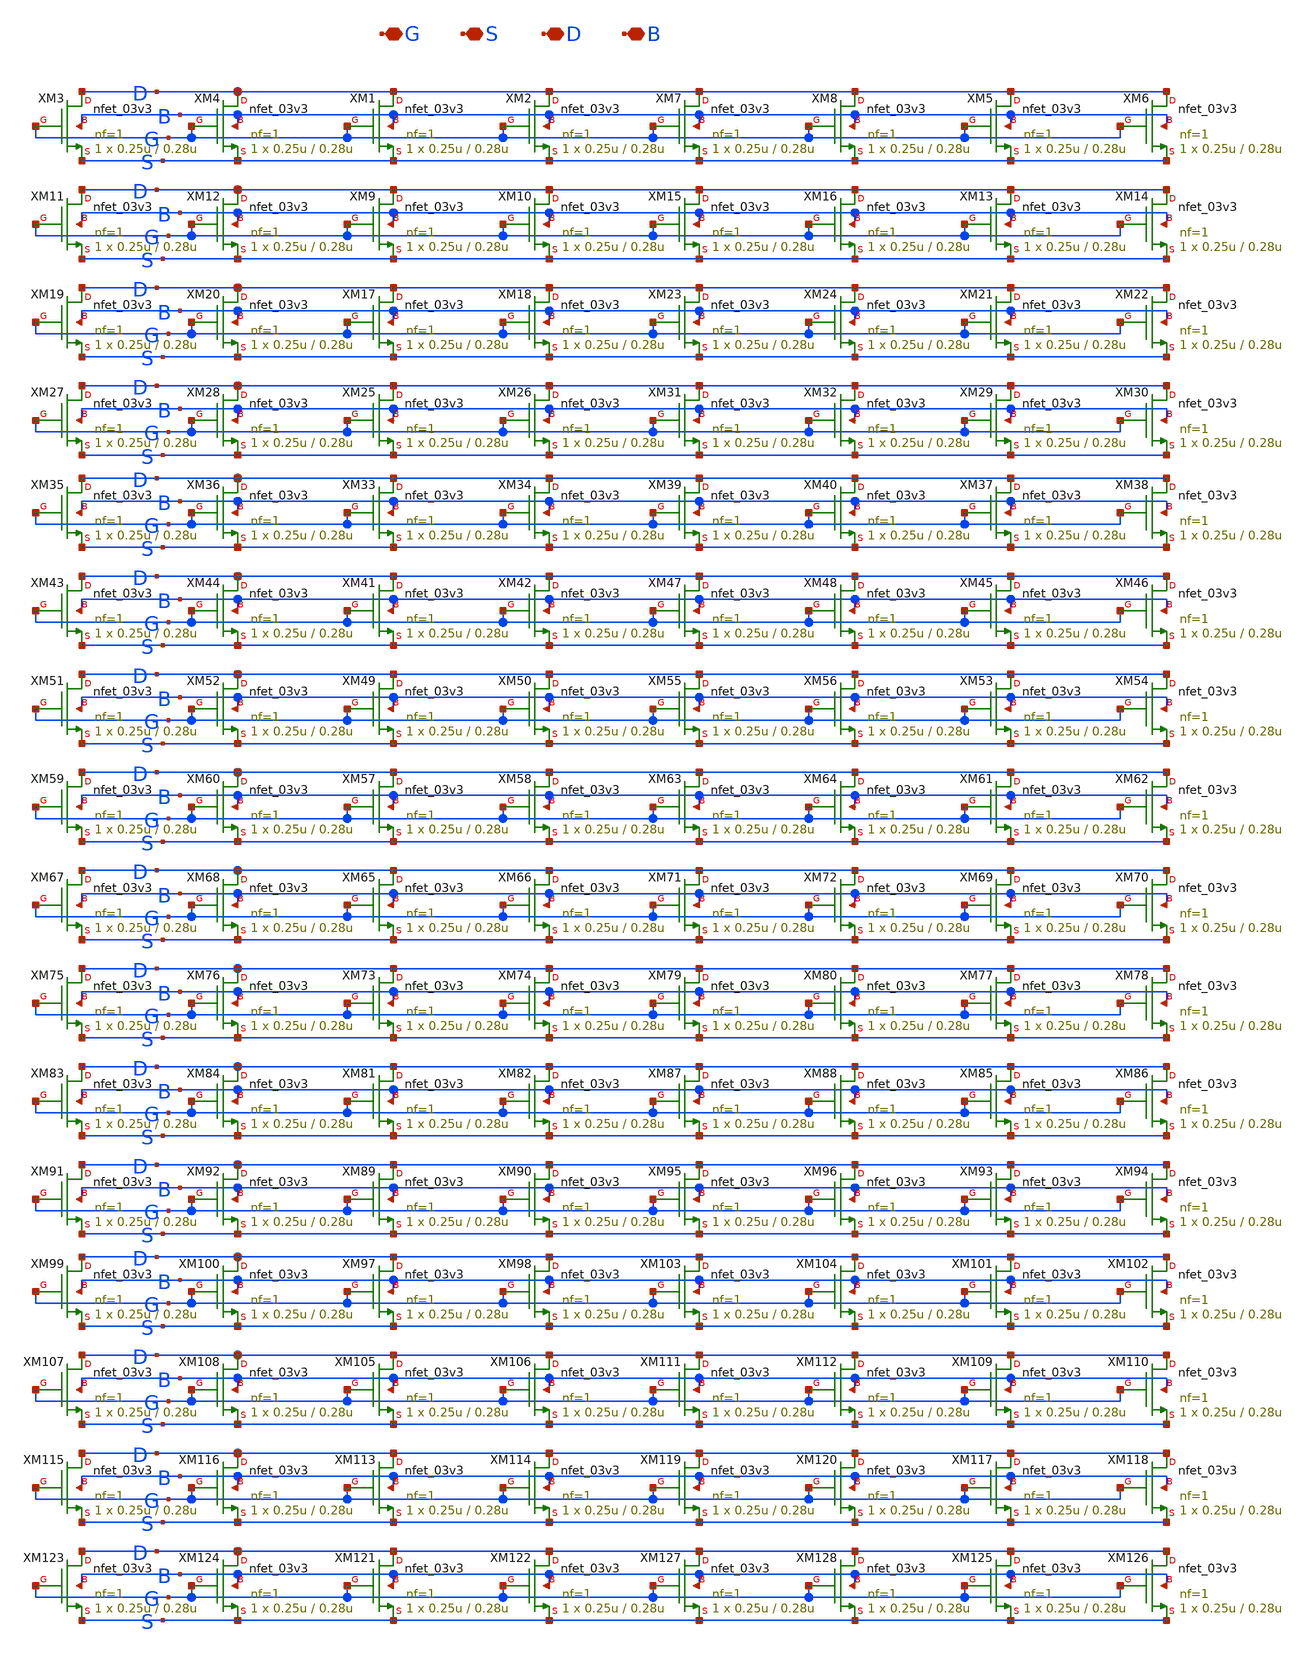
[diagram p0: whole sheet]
** sch_path: DAC_PAKISTAN_01/Pakistan1_Xschem/nfet_03V3_m128.sch
**.subckt nfet_03V3_m128 G S D B
*.iopin G
*.iopin S
*.iopin D
*.iopin B
XM1 D G S B nfet_03v3 L=0.28u W=0.25u nf=1 ad='int((nf+1)/2) * W/nf * 0.18u' as='int((nf+2)/2) * W/nf * 0.18u'
+ pd='2*int((nf+1)/2) * (W/nf + 0.18u)' ps='2*int((nf+2)/2) * (W/nf + 0.18u)' nrd='0.18u / W' nrs='0.18u / W'
+ sa=0 sb=0 sd=0 m=1
XM2 D G S B nfet_03v3 L=0.28u W=0.25u nf=1 ad='int((nf+1)/2) * W/nf * 0.18u' as='int((nf+2)/2) * W/nf * 0.18u'
+ pd='2*int((nf+1)/2) * (W/nf + 0.18u)' ps='2*int((nf+2)/2) * (W/nf + 0.18u)' nrd='0.18u / W' nrs='0.18u / W'
+ sa=0 sb=0 sd=0 m=1
XM3 D G S B nfet_03v3 L=0.28u W=0.25u nf=1 ad='int((nf+1)/2) * W/nf * 0.18u' as='int((nf+2)/2) * W/nf * 0.18u'
+ pd='2*int((nf+1)/2) * (W/nf + 0.18u)' ps='2*int((nf+2)/2) * (W/nf + 0.18u)' nrd='0.18u / W' nrs='0.18u / W'
+ sa=0 sb=0 sd=0 m=1
XM4 D G S B nfet_03v3 L=0.28u W=0.25u nf=1 ad='int((nf+1)/2) * W/nf * 0.18u' as='int((nf+2)/2) * W/nf * 0.18u'
+ pd='2*int((nf+1)/2) * (W/nf + 0.18u)' ps='2*int((nf+2)/2) * (W/nf + 0.18u)' nrd='0.18u / W' nrs='0.18u / W'
+ sa=0 sb=0 sd=0 m=1
XM5 D G S B nfet_03v3 L=0.28u W=0.25u nf=1 ad='int((nf+1)/2) * W/nf * 0.18u' as='int((nf+2)/2) * W/nf * 0.18u'
+ pd='2*int((nf+1)/2) * (W/nf + 0.18u)' ps='2*int((nf+2)/2) * (W/nf + 0.18u)' nrd='0.18u / W' nrs='0.18u / W'
+ sa=0 sb=0 sd=0 m=1
XM6 D G S B nfet_03v3 L=0.28u W=0.25u nf=1 ad='int((nf+1)/2) * W/nf * 0.18u' as='int((nf+2)/2) * W/nf * 0.18u'
+ pd='2*int((nf+1)/2) * (W/nf + 0.18u)' ps='2*int((nf+2)/2) * (W/nf + 0.18u)' nrd='0.18u / W' nrs='0.18u / W'
+ sa=0 sb=0 sd=0 m=1
XM7 D G S B nfet_03v3 L=0.28u W=0.25u nf=1 ad='int((nf+1)/2) * W/nf * 0.18u' as='int((nf+2)/2) * W/nf * 0.18u'
+ pd='2*int((nf+1)/2) * (W/nf + 0.18u)' ps='2*int((nf+2)/2) * (W/nf + 0.18u)' nrd='0.18u / W' nrs='0.18u / W'
+ sa=0 sb=0 sd=0 m=1
XM8 D G S B nfet_03v3 L=0.28u W=0.25u nf=1 ad='int((nf+1)/2) * W/nf * 0.18u' as='int((nf+2)/2) * W/nf * 0.18u'
+ pd='2*int((nf+1)/2) * (W/nf + 0.18u)' ps='2*int((nf+2)/2) * (W/nf + 0.18u)' nrd='0.18u / W' nrs='0.18u / W'
+ sa=0 sb=0 sd=0 m=1
XM9 D G S B nfet_03v3 L=0.28u W=0.25u nf=1 ad='int((nf+1)/2) * W/nf * 0.18u' as='int((nf+2)/2) * W/nf * 0.18u'
+ pd='2*int((nf+1)/2) * (W/nf + 0.18u)' ps='2*int((nf+2)/2) * (W/nf + 0.18u)' nrd='0.18u / W' nrs='0.18u / W'
+ sa=0 sb=0 sd=0 m=1
XM10 D G S B nfet_03v3 L=0.28u W=0.25u nf=1 ad='int((nf+1)/2) * W/nf * 0.18u' as='int((nf+2)/2) * W/nf * 0.18u'
+ pd='2*int((nf+1)/2) * (W/nf + 0.18u)' ps='2*int((nf+2)/2) * (W/nf + 0.18u)' nrd='0.18u / W' nrs='0.18u / W'
+ sa=0 sb=0 sd=0 m=1
XM11 D G S B nfet_03v3 L=0.28u W=0.25u nf=1 ad='int((nf+1)/2) * W/nf * 0.18u' as='int((nf+2)/2) * W/nf * 0.18u'
+ pd='2*int((nf+1)/2) * (W/nf + 0.18u)' ps='2*int((nf+2)/2) * (W/nf + 0.18u)' nrd='0.18u / W' nrs='0.18u / W'
+ sa=0 sb=0 sd=0 m=1
XM12 D G S B nfet_03v3 L=0.28u W=0.25u nf=1 ad='int((nf+1)/2) * W/nf * 0.18u' as='int((nf+2)/2) * W/nf * 0.18u'
+ pd='2*int((nf+1)/2) * (W/nf + 0.18u)' ps='2*int((nf+2)/2) * (W/nf + 0.18u)' nrd='0.18u / W' nrs='0.18u / W'
+ sa=0 sb=0 sd=0 m=1
XM13 D G S B nfet_03v3 L=0.28u W=0.25u nf=1 ad='int((nf+1)/2) * W/nf * 0.18u' as='int((nf+2)/2) * W/nf * 0.18u'
+ pd='2*int((nf+1)/2) * (W/nf + 0.18u)' ps='2*int((nf+2)/2) * (W/nf + 0.18u)' nrd='0.18u / W' nrs='0.18u / W'
+ sa=0 sb=0 sd=0 m=1
XM14 D G S B nfet_03v3 L=0.28u W=0.25u nf=1 ad='int((nf+1)/2) * W/nf * 0.18u' as='int((nf+2)/2) * W/nf * 0.18u'
+ pd='2*int((nf+1)/2) * (W/nf + 0.18u)' ps='2*int((nf+2)/2) * (W/nf + 0.18u)' nrd='0.18u / W' nrs='0.18u / W'
+ sa=0 sb=0 sd=0 m=1
XM15 D G S B nfet_03v3 L=0.28u W=0.25u nf=1 ad='int((nf+1)/2) * W/nf * 0.18u' as='int((nf+2)/2) * W/nf * 0.18u'
+ pd='2*int((nf+1)/2) * (W/nf + 0.18u)' ps='2*int((nf+2)/2) * (W/nf + 0.18u)' nrd='0.18u / W' nrs='0.18u / W'
+ sa=0 sb=0 sd=0 m=1
XM16 D G S B nfet_03v3 L=0.28u W=0.25u nf=1 ad='int((nf+1)/2) * W/nf * 0.18u' as='int((nf+2)/2) * W/nf * 0.18u'
+ pd='2*int((nf+1)/2) * (W/nf + 0.18u)' ps='2*int((nf+2)/2) * (W/nf + 0.18u)' nrd='0.18u / W' nrs='0.18u / W'
+ sa=0 sb=0 sd=0 m=1
XM17 D G S B nfet_03v3 L=0.28u W=0.25u nf=1 ad='int((nf+1)/2) * W/nf * 0.18u' as='int((nf+2)/2) * W/nf * 0.18u'
+ pd='2*int((nf+1)/2) * (W/nf + 0.18u)' ps='2*int((nf+2)/2) * (W/nf + 0.18u)' nrd='0.18u / W' nrs='0.18u / W'
+ sa=0 sb=0 sd=0 m=1
XM18 D G S B nfet_03v3 L=0.28u W=0.25u nf=1 ad='int((nf+1)/2) * W/nf * 0.18u' as='int((nf+2)/2) * W/nf * 0.18u'
+ pd='2*int((nf+1)/2) * (W/nf + 0.18u)' ps='2*int((nf+2)/2) * (W/nf + 0.18u)' nrd='0.18u / W' nrs='0.18u / W'
+ sa=0 sb=0 sd=0 m=1
XM19 D G S B nfet_03v3 L=0.28u W=0.25u nf=1 ad='int((nf+1)/2) * W/nf * 0.18u' as='int((nf+2)/2) * W/nf * 0.18u'
+ pd='2*int((nf+1)/2) * (W/nf + 0.18u)' ps='2*int((nf+2)/2) * (W/nf + 0.18u)' nrd='0.18u / W' nrs='0.18u / W'
+ sa=0 sb=0 sd=0 m=1
XM20 D G S B nfet_03v3 L=0.28u W=0.25u nf=1 ad='int((nf+1)/2) * W/nf * 0.18u' as='int((nf+2)/2) * W/nf * 0.18u'
+ pd='2*int((nf+1)/2) * (W/nf + 0.18u)' ps='2*int((nf+2)/2) * (W/nf + 0.18u)' nrd='0.18u / W' nrs='0.18u / W'
+ sa=0 sb=0 sd=0 m=1
XM21 D G S B nfet_03v3 L=0.28u W=0.25u nf=1 ad='int((nf+1)/2) * W/nf * 0.18u' as='int((nf+2)/2) * W/nf * 0.18u'
+ pd='2*int((nf+1)/2) * (W/nf + 0.18u)' ps='2*int((nf+2)/2) * (W/nf + 0.18u)' nrd='0.18u / W' nrs='0.18u / W'
+ sa=0 sb=0 sd=0 m=1
XM22 D G S B nfet_03v3 L=0.28u W=0.25u nf=1 ad='int((nf+1)/2) * W/nf * 0.18u' as='int((nf+2)/2) * W/nf * 0.18u'
+ pd='2*int((nf+1)/2) * (W/nf + 0.18u)' ps='2*int((nf+2)/2) * (W/nf + 0.18u)' nrd='0.18u / W' nrs='0.18u / W'
+ sa=0 sb=0 sd=0 m=1
XM23 D G S B nfet_03v3 L=0.28u W=0.25u nf=1 ad='int((nf+1)/2) * W/nf * 0.18u' as='int((nf+2)/2) * W/nf * 0.18u'
+ pd='2*int((nf+1)/2) * (W/nf + 0.18u)' ps='2*int((nf+2)/2) * (W/nf + 0.18u)' nrd='0.18u / W' nrs='0.18u / W'
+ sa=0 sb=0 sd=0 m=1
XM24 D G S B nfet_03v3 L=0.28u W=0.25u nf=1 ad='int((nf+1)/2) * W/nf * 0.18u' as='int((nf+2)/2) * W/nf * 0.18u'
+ pd='2*int((nf+1)/2) * (W/nf + 0.18u)' ps='2*int((nf+2)/2) * (W/nf + 0.18u)' nrd='0.18u / W' nrs='0.18u / W'
+ sa=0 sb=0 sd=0 m=1
XM25 D G S B nfet_03v3 L=0.28u W=0.25u nf=1 ad='int((nf+1)/2) * W/nf * 0.18u' as='int((nf+2)/2) * W/nf * 0.18u'
+ pd='2*int((nf+1)/2) * (W/nf + 0.18u)' ps='2*int((nf+2)/2) * (W/nf + 0.18u)' nrd='0.18u / W' nrs='0.18u / W'
+ sa=0 sb=0 sd=0 m=1
XM26 D G S B nfet_03v3 L=0.28u W=0.25u nf=1 ad='int((nf+1)/2) * W/nf * 0.18u' as='int((nf+2)/2) * W/nf * 0.18u'
+ pd='2*int((nf+1)/2) * (W/nf + 0.18u)' ps='2*int((nf+2)/2) * (W/nf + 0.18u)' nrd='0.18u / W' nrs='0.18u / W'
+ sa=0 sb=0 sd=0 m=1
XM27 D G S B nfet_03v3 L=0.28u W=0.25u nf=1 ad='int((nf+1)/2) * W/nf * 0.18u' as='int((nf+2)/2) * W/nf * 0.18u'
+ pd='2*int((nf+1)/2) * (W/nf + 0.18u)' ps='2*int((nf+2)/2) * (W/nf + 0.18u)' nrd='0.18u / W' nrs='0.18u / W'
+ sa=0 sb=0 sd=0 m=1
XM28 D G S B nfet_03v3 L=0.28u W=0.25u nf=1 ad='int((nf+1)/2) * W/nf * 0.18u' as='int((nf+2)/2) * W/nf * 0.18u'
+ pd='2*int((nf+1)/2) * (W/nf + 0.18u)' ps='2*int((nf+2)/2) * (W/nf + 0.18u)' nrd='0.18u / W' nrs='0.18u / W'
+ sa=0 sb=0 sd=0 m=1
XM29 D G S B nfet_03v3 L=0.28u W=0.25u nf=1 ad='int((nf+1)/2) * W/nf * 0.18u' as='int((nf+2)/2) * W/nf * 0.18u'
+ pd='2*int((nf+1)/2) * (W/nf + 0.18u)' ps='2*int((nf+2)/2) * (W/nf + 0.18u)' nrd='0.18u / W' nrs='0.18u / W'
+ sa=0 sb=0 sd=0 m=1
XM30 D G S B nfet_03v3 L=0.28u W=0.25u nf=1 ad='int((nf+1)/2) * W/nf * 0.18u' as='int((nf+2)/2) * W/nf * 0.18u'
+ pd='2*int((nf+1)/2) * (W/nf + 0.18u)' ps='2*int((nf+2)/2) * (W/nf + 0.18u)' nrd='0.18u / W' nrs='0.18u / W'
+ sa=0 sb=0 sd=0 m=1
XM31 D G S B nfet_03v3 L=0.28u W=0.25u nf=1 ad='int((nf+1)/2) * W/nf * 0.18u' as='int((nf+2)/2) * W/nf * 0.18u'
+ pd='2*int((nf+1)/2) * (W/nf + 0.18u)' ps='2*int((nf+2)/2) * (W/nf + 0.18u)' nrd='0.18u / W' nrs='0.18u / W'
+ sa=0 sb=0 sd=0 m=1
XM32 D G S B nfet_03v3 L=0.28u W=0.25u nf=1 ad='int((nf+1)/2) * W/nf * 0.18u' as='int((nf+2)/2) * W/nf * 0.18u'
+ pd='2*int((nf+1)/2) * (W/nf + 0.18u)' ps='2*int((nf+2)/2) * (W/nf + 0.18u)' nrd='0.18u / W' nrs='0.18u / W'
+ sa=0 sb=0 sd=0 m=1
XM33 D G S B nfet_03v3 L=0.28u W=0.25u nf=1 ad='int((nf+1)/2) * W/nf * 0.18u' as='int((nf+2)/2) * W/nf * 0.18u'
+ pd='2*int((nf+1)/2) * (W/nf + 0.18u)' ps='2*int((nf+2)/2) * (W/nf + 0.18u)' nrd='0.18u / W' nrs='0.18u / W'
+ sa=0 sb=0 sd=0 m=1
XM34 D G S B nfet_03v3 L=0.28u W=0.25u nf=1 ad='int((nf+1)/2) * W/nf * 0.18u' as='int((nf+2)/2) * W/nf * 0.18u'
+ pd='2*int((nf+1)/2) * (W/nf + 0.18u)' ps='2*int((nf+2)/2) * (W/nf + 0.18u)' nrd='0.18u / W' nrs='0.18u / W'
+ sa=0 sb=0 sd=0 m=1
XM35 D G S B nfet_03v3 L=0.28u W=0.25u nf=1 ad='int((nf+1)/2) * W/nf * 0.18u' as='int((nf+2)/2) * W/nf * 0.18u'
+ pd='2*int((nf+1)/2) * (W/nf + 0.18u)' ps='2*int((nf+2)/2) * (W/nf + 0.18u)' nrd='0.18u / W' nrs='0.18u / W'
+ sa=0 sb=0 sd=0 m=1
XM36 D G S B nfet_03v3 L=0.28u W=0.25u nf=1 ad='int((nf+1)/2) * W/nf * 0.18u' as='int((nf+2)/2) * W/nf * 0.18u'
+ pd='2*int((nf+1)/2) * (W/nf + 0.18u)' ps='2*int((nf+2)/2) * (W/nf + 0.18u)' nrd='0.18u / W' nrs='0.18u / W'
+ sa=0 sb=0 sd=0 m=1
XM37 D G S B nfet_03v3 L=0.28u W=0.25u nf=1 ad='int((nf+1)/2) * W/nf * 0.18u' as='int((nf+2)/2) * W/nf * 0.18u'
+ pd='2*int((nf+1)/2) * (W/nf + 0.18u)' ps='2*int((nf+2)/2) * (W/nf + 0.18u)' nrd='0.18u / W' nrs='0.18u / W'
+ sa=0 sb=0 sd=0 m=1
XM38 D G S B nfet_03v3 L=0.28u W=0.25u nf=1 ad='int((nf+1)/2) * W/nf * 0.18u' as='int((nf+2)/2) * W/nf * 0.18u'
+ pd='2*int((nf+1)/2) * (W/nf + 0.18u)' ps='2*int((nf+2)/2) * (W/nf + 0.18u)' nrd='0.18u / W' nrs='0.18u / W'
+ sa=0 sb=0 sd=0 m=1
XM39 D G S B nfet_03v3 L=0.28u W=0.25u nf=1 ad='int((nf+1)/2) * W/nf * 0.18u' as='int((nf+2)/2) * W/nf * 0.18u'
+ pd='2*int((nf+1)/2) * (W/nf + 0.18u)' ps='2*int((nf+2)/2) * (W/nf + 0.18u)' nrd='0.18u / W' nrs='0.18u / W'
+ sa=0 sb=0 sd=0 m=1
XM40 D G S B nfet_03v3 L=0.28u W=0.25u nf=1 ad='int((nf+1)/2) * W/nf * 0.18u' as='int((nf+2)/2) * W/nf * 0.18u'
+ pd='2*int((nf+1)/2) * (W/nf + 0.18u)' ps='2*int((nf+2)/2) * (W/nf + 0.18u)' nrd='0.18u / W' nrs='0.18u / W'
+ sa=0 sb=0 sd=0 m=1
XM41 D G S B nfet_03v3 L=0.28u W=0.25u nf=1 ad='int((nf+1)/2) * W/nf * 0.18u' as='int((nf+2)/2) * W/nf * 0.18u'
+ pd='2*int((nf+1)/2) * (W/nf + 0.18u)' ps='2*int((nf+2)/2) * (W/nf + 0.18u)' nrd='0.18u / W' nrs='0.18u / W'
+ sa=0 sb=0 sd=0 m=1
XM42 D G S B nfet_03v3 L=0.28u W=0.25u nf=1 ad='int((nf+1)/2) * W/nf * 0.18u' as='int((nf+2)/2) * W/nf * 0.18u'
+ pd='2*int((nf+1)/2) * (W/nf + 0.18u)' ps='2*int((nf+2)/2) * (W/nf + 0.18u)' nrd='0.18u / W' nrs='0.18u / W'
+ sa=0 sb=0 sd=0 m=1
XM43 D G S B nfet_03v3 L=0.28u W=0.25u nf=1 ad='int((nf+1)/2) * W/nf * 0.18u' as='int((nf+2)/2) * W/nf * 0.18u'
+ pd='2*int((nf+1)/2) * (W/nf + 0.18u)' ps='2*int((nf+2)/2) * (W/nf + 0.18u)' nrd='0.18u / W' nrs='0.18u / W'
+ sa=0 sb=0 sd=0 m=1
XM44 D G S B nfet_03v3 L=0.28u W=0.25u nf=1 ad='int((nf+1)/2) * W/nf * 0.18u' as='int((nf+2)/2) * W/nf * 0.18u'
+ pd='2*int((nf+1)/2) * (W/nf + 0.18u)' ps='2*int((nf+2)/2) * (W/nf + 0.18u)' nrd='0.18u / W' nrs='0.18u / W'
+ sa=0 sb=0 sd=0 m=1
XM45 D G S B nfet_03v3 L=0.28u W=0.25u nf=1 ad='int((nf+1)/2) * W/nf * 0.18u' as='int((nf+2)/2) * W/nf * 0.18u'
+ pd='2*int((nf+1)/2) * (W/nf + 0.18u)' ps='2*int((nf+2)/2) * (W/nf + 0.18u)' nrd='0.18u / W' nrs='0.18u / W'
+ sa=0 sb=0 sd=0 m=1
XM46 D G S B nfet_03v3 L=0.28u W=0.25u nf=1 ad='int((nf+1)/2) * W/nf * 0.18u' as='int((nf+2)/2) * W/nf * 0.18u'
+ pd='2*int((nf+1)/2) * (W/nf + 0.18u)' ps='2*int((nf+2)/2) * (W/nf + 0.18u)' nrd='0.18u / W' nrs='0.18u / W'
+ sa=0 sb=0 sd=0 m=1
XM47 D G S B nfet_03v3 L=0.28u W=0.25u nf=1 ad='int((nf+1)/2) * W/nf * 0.18u' as='int((nf+2)/2) * W/nf * 0.18u'
+ pd='2*int((nf+1)/2) * (W/nf + 0.18u)' ps='2*int((nf+2)/2) * (W/nf + 0.18u)' nrd='0.18u / W' nrs='0.18u / W'
+ sa=0 sb=0 sd=0 m=1
XM48 D G S B nfet_03v3 L=0.28u W=0.25u nf=1 ad='int((nf+1)/2) * W/nf * 0.18u' as='int((nf+2)/2) * W/nf * 0.18u'
+ pd='2*int((nf+1)/2) * (W/nf + 0.18u)' ps='2*int((nf+2)/2) * (W/nf + 0.18u)' nrd='0.18u / W' nrs='0.18u / W'
+ sa=0 sb=0 sd=0 m=1
XM49 D G S B nfet_03v3 L=0.28u W=0.25u nf=1 ad='int((nf+1)/2) * W/nf * 0.18u' as='int((nf+2)/2) * W/nf * 0.18u'
+ pd='2*int((nf+1)/2) * (W/nf + 0.18u)' ps='2*int((nf+2)/2) * (W/nf + 0.18u)' nrd='0.18u / W' nrs='0.18u / W'
+ sa=0 sb=0 sd=0 m=1
XM50 D G S B nfet_03v3 L=0.28u W=0.25u nf=1 ad='int((nf+1)/2) * W/nf * 0.18u' as='int((nf+2)/2) * W/nf * 0.18u'
+ pd='2*int((nf+1)/2) * (W/nf + 0.18u)' ps='2*int((nf+2)/2) * (W/nf + 0.18u)' nrd='0.18u / W' nrs='0.18u / W'
+ sa=0 sb=0 sd=0 m=1
XM51 D G S B nfet_03v3 L=0.28u W=0.25u nf=1 ad='int((nf+1)/2) * W/nf * 0.18u' as='int((nf+2)/2) * W/nf * 0.18u'
+ pd='2*int((nf+1)/2) * (W/nf + 0.18u)' ps='2*int((nf+2)/2) * (W/nf + 0.18u)' nrd='0.18u / W' nrs='0.18u / W'
+ sa=0 sb=0 sd=0 m=1
XM52 D G S B nfet_03v3 L=0.28u W=0.25u nf=1 ad='int((nf+1)/2) * W/nf * 0.18u' as='int((nf+2)/2) * W/nf * 0.18u'
+ pd='2*int((nf+1)/2) * (W/nf + 0.18u)' ps='2*int((nf+2)/2) * (W/nf + 0.18u)' nrd='0.18u / W' nrs='0.18u / W'
+ sa=0 sb=0 sd=0 m=1
XM53 D G S B nfet_03v3 L=0.28u W=0.25u nf=1 ad='int((nf+1)/2) * W/nf * 0.18u' as='int((nf+2)/2) * W/nf * 0.18u'
+ pd='2*int((nf+1)/2) * (W/nf + 0.18u)' ps='2*int((nf+2)/2) * (W/nf + 0.18u)' nrd='0.18u / W' nrs='0.18u / W'
+ sa=0 sb=0 sd=0 m=1
XM54 D G S B nfet_03v3 L=0.28u W=0.25u nf=1 ad='int((nf+1)/2) * W/nf * 0.18u' as='int((nf+2)/2) * W/nf * 0.18u'
+ pd='2*int((nf+1)/2) * (W/nf + 0.18u)' ps='2*int((nf+2)/2) * (W/nf + 0.18u)' nrd='0.18u / W' nrs='0.18u / W'
+ sa=0 sb=0 sd=0 m=1
XM55 D G S B nfet_03v3 L=0.28u W=0.25u nf=1 ad='int((nf+1)/2) * W/nf * 0.18u' as='int((nf+2)/2) * W/nf * 0.18u'
+ pd='2*int((nf+1)/2) * (W/nf + 0.18u)' ps='2*int((nf+2)/2) * (W/nf + 0.18u)' nrd='0.18u / W' nrs='0.18u / W'
+ sa=0 sb=0 sd=0 m=1
XM56 D G S B nfet_03v3 L=0.28u W=0.25u nf=1 ad='int((nf+1)/2) * W/nf * 0.18u' as='int((nf+2)/2) * W/nf * 0.18u'
+ pd='2*int((nf+1)/2) * (W/nf + 0.18u)' ps='2*int((nf+2)/2) * (W/nf + 0.18u)' nrd='0.18u / W' nrs='0.18u / W'
+ sa=0 sb=0 sd=0 m=1
XM57 D G S B nfet_03v3 L=0.28u W=0.25u nf=1 ad='int((nf+1)/2) * W/nf * 0.18u' as='int((nf+2)/2) * W/nf * 0.18u'
+ pd='2*int((nf+1)/2) * (W/nf + 0.18u)' ps='2*int((nf+2)/2) * (W/nf + 0.18u)' nrd='0.18u / W' nrs='0.18u / W'
+ sa=0 sb=0 sd=0 m=1
XM58 D G S B nfet_03v3 L=0.28u W=0.25u nf=1 ad='int((nf+1)/2) * W/nf * 0.18u' as='int((nf+2)/2) * W/nf * 0.18u'
+ pd='2*int((nf+1)/2) * (W/nf + 0.18u)' ps='2*int((nf+2)/2) * (W/nf + 0.18u)' nrd='0.18u / W' nrs='0.18u / W'
+ sa=0 sb=0 sd=0 m=1
XM59 D G S B nfet_03v3 L=0.28u W=0.25u nf=1 ad='int((nf+1)/2) * W/nf * 0.18u' as='int((nf+2)/2) * W/nf * 0.18u'
+ pd='2*int((nf+1)/2) * (W/nf + 0.18u)' ps='2*int((nf+2)/2) * (W/nf + 0.18u)' nrd='0.18u / W' nrs='0.18u / W'
+ sa=0 sb=0 sd=0 m=1
XM60 D G S B nfet_03v3 L=0.28u W=0.25u nf=1 ad='int((nf+1)/2) * W/nf * 0.18u' as='int((nf+2)/2) * W/nf * 0.18u'
+ pd='2*int((nf+1)/2) * (W/nf + 0.18u)' ps='2*int((nf+2)/2) * (W/nf + 0.18u)' nrd='0.18u / W' nrs='0.18u / W'
+ sa=0 sb=0 sd=0 m=1
XM61 D G S B nfet_03v3 L=0.28u W=0.25u nf=1 ad='int((nf+1)/2) * W/nf * 0.18u' as='int((nf+2)/2) * W/nf * 0.18u'
+ pd='2*int((nf+1)/2) * (W/nf + 0.18u)' ps='2*int((nf+2)/2) * (W/nf + 0.18u)' nrd='0.18u / W' nrs='0.18u / W'
+ sa=0 sb=0 sd=0 m=1
XM62 D G S B nfet_03v3 L=0.28u W=0.25u nf=1 ad='int((nf+1)/2) * W/nf * 0.18u' as='int((nf+2)/2) * W/nf * 0.18u'
+ pd='2*int((nf+1)/2) * (W/nf + 0.18u)' ps='2*int((nf+2)/2) * (W/nf + 0.18u)' nrd='0.18u / W' nrs='0.18u / W'
+ sa=0 sb=0 sd=0 m=1
XM63 D G S B nfet_03v3 L=0.28u W=0.25u nf=1 ad='int((nf+1)/2) * W/nf * 0.18u' as='int((nf+2)/2) * W/nf * 0.18u'
+ pd='2*int((nf+1)/2) * (W/nf + 0.18u)' ps='2*int((nf+2)/2) * (W/nf + 0.18u)' nrd='0.18u / W' nrs='0.18u / W'
+ sa=0 sb=0 sd=0 m=1
XM64 D G S B nfet_03v3 L=0.28u W=0.25u nf=1 ad='int((nf+1)/2) * W/nf * 0.18u' as='int((nf+2)/2) * W/nf * 0.18u'
+ pd='2*int((nf+1)/2) * (W/nf + 0.18u)' ps='2*int((nf+2)/2) * (W/nf + 0.18u)' nrd='0.18u / W' nrs='0.18u / W'
+ sa=0 sb=0 sd=0 m=1
XM65 D G S B nfet_03v3 L=0.28u W=0.25u nf=1 ad='int((nf+1)/2) * W/nf * 0.18u' as='int((nf+2)/2) * W/nf * 0.18u'
+ pd='2*int((nf+1)/2) * (W/nf + 0.18u)' ps='2*int((nf+2)/2) * (W/nf + 0.18u)' nrd='0.18u / W' nrs='0.18u / W'
+ sa=0 sb=0 sd=0 m=1
XM66 D G S B nfet_03v3 L=0.28u W=0.25u nf=1 ad='int((nf+1)/2) * W/nf * 0.18u' as='int((nf+2)/2) * W/nf * 0.18u'
+ pd='2*int((nf+1)/2) * (W/nf + 0.18u)' ps='2*int((nf+2)/2) * (W/nf + 0.18u)' nrd='0.18u / W' nrs='0.18u / W'
+ sa=0 sb=0 sd=0 m=1
XM67 D G S B nfet_03v3 L=0.28u W=0.25u nf=1 ad='int((nf+1)/2) * W/nf * 0.18u' as='int((nf+2)/2) * W/nf * 0.18u'
+ pd='2*int((nf+1)/2) * (W/nf + 0.18u)' ps='2*int((nf+2)/2) * (W/nf + 0.18u)' nrd='0.18u / W' nrs='0.18u / W'
+ sa=0 sb=0 sd=0 m=1
XM68 D G S B nfet_03v3 L=0.28u W=0.25u nf=1 ad='int((nf+1)/2) * W/nf * 0.18u' as='int((nf+2)/2) * W/nf * 0.18u'
+ pd='2*int((nf+1)/2) * (W/nf + 0.18u)' ps='2*int((nf+2)/2) * (W/nf + 0.18u)' nrd='0.18u / W' nrs='0.18u / W'
+ sa=0 sb=0 sd=0 m=1
XM69 D G S B nfet_03v3 L=0.28u W=0.25u nf=1 ad='int((nf+1)/2) * W/nf * 0.18u' as='int((nf+2)/2) * W/nf * 0.18u'
+ pd='2*int((nf+1)/2) * (W/nf + 0.18u)' ps='2*int((nf+2)/2) * (W/nf + 0.18u)' nrd='0.18u / W' nrs='0.18u / W'
+ sa=0 sb=0 sd=0 m=1
XM70 D G S B nfet_03v3 L=0.28u W=0.25u nf=1 ad='int((nf+1)/2) * W/nf * 0.18u' as='int((nf+2)/2) * W/nf * 0.18u'
+ pd='2*int((nf+1)/2) * (W/nf + 0.18u)' ps='2*int((nf+2)/2) * (W/nf + 0.18u)' nrd='0.18u / W' nrs='0.18u / W'
+ sa=0 sb=0 sd=0 m=1
XM71 D G S B nfet_03v3 L=0.28u W=0.25u nf=1 ad='int((nf+1)/2) * W/nf * 0.18u' as='int((nf+2)/2) * W/nf * 0.18u'
+ pd='2*int((nf+1)/2) * (W/nf + 0.18u)' ps='2*int((nf+2)/2) * (W/nf + 0.18u)' nrd='0.18u / W' nrs='0.18u / W'
+ sa=0 sb=0 sd=0 m=1
XM72 D G S B nfet_03v3 L=0.28u W=0.25u nf=1 ad='int((nf+1)/2) * W/nf * 0.18u' as='int((nf+2)/2) * W/nf * 0.18u'
+ pd='2*int((nf+1)/2) * (W/nf + 0.18u)' ps='2*int((nf+2)/2) * (W/nf + 0.18u)' nrd='0.18u / W' nrs='0.18u / W'
+ sa=0 sb=0 sd=0 m=1
XM73 D G S B nfet_03v3 L=0.28u W=0.25u nf=1 ad='int((nf+1)/2) * W/nf * 0.18u' as='int((nf+2)/2) * W/nf * 0.18u'
+ pd='2*int((nf+1)/2) * (W/nf + 0.18u)' ps='2*int((nf+2)/2) * (W/nf + 0.18u)' nrd='0.18u / W' nrs='0.18u / W'
+ sa=0 sb=0 sd=0 m=1
XM74 D G S B nfet_03v3 L=0.28u W=0.25u nf=1 ad='int((nf+1)/2) * W/nf * 0.18u' as='int((nf+2)/2) * W/nf * 0.18u'
+ pd='2*int((nf+1)/2) * (W/nf + 0.18u)' ps='2*int((nf+2)/2) * (W/nf + 0.18u)' nrd='0.18u / W' nrs='0.18u / W'
+ sa=0 sb=0 sd=0 m=1
XM75 D G S B nfet_03v3 L=0.28u W=0.25u nf=1 ad='int((nf+1)/2) * W/nf * 0.18u' as='int((nf+2)/2) * W/nf * 0.18u'
+ pd='2*int((nf+1)/2) * (W/nf + 0.18u)' ps='2*int((nf+2)/2) * (W/nf + 0.18u)' nrd='0.18u / W' nrs='0.18u / W'
+ sa=0 sb=0 sd=0 m=1
XM76 D G S B nfet_03v3 L=0.28u W=0.25u nf=1 ad='int((nf+1)/2) * W/nf * 0.18u' as='int((nf+2)/2) * W/nf * 0.18u'
+ pd='2*int((nf+1)/2) * (W/nf + 0.18u)' ps='2*int((nf+2)/2) * (W/nf + 0.18u)' nrd='0.18u / W' nrs='0.18u / W'
+ sa=0 sb=0 sd=0 m=1
XM77 D G S B nfet_03v3 L=0.28u W=0.25u nf=1 ad='int((nf+1)/2) * W/nf * 0.18u' as='int((nf+2)/2) * W/nf * 0.18u'
+ pd='2*int((nf+1)/2) * (W/nf + 0.18u)' ps='2*int((nf+2)/2) * (W/nf + 0.18u)' nrd='0.18u / W' nrs='0.18u / W'
+ sa=0 sb=0 sd=0 m=1
XM78 D G S B nfet_03v3 L=0.28u W=0.25u nf=1 ad='int((nf+1)/2) * W/nf * 0.18u' as='int((nf+2)/2) * W/nf * 0.18u'
+ pd='2*int((nf+1)/2) * (W/nf + 0.18u)' ps='2*int((nf+2)/2) * (W/nf + 0.18u)' nrd='0.18u / W' nrs='0.18u / W'
+ sa=0 sb=0 sd=0 m=1
XM79 D G S B nfet_03v3 L=0.28u W=0.25u nf=1 ad='int((nf+1)/2) * W/nf * 0.18u' as='int((nf+2)/2) * W/nf * 0.18u'
+ pd='2*int((nf+1)/2) * (W/nf + 0.18u)' ps='2*int((nf+2)/2) * (W/nf + 0.18u)' nrd='0.18u / W' nrs='0.18u / W'
+ sa=0 sb=0 sd=0 m=1
XM80 D G S B nfet_03v3 L=0.28u W=0.25u nf=1 ad='int((nf+1)/2) * W/nf * 0.18u' as='int((nf+2)/2) * W/nf * 0.18u'
+ pd='2*int((nf+1)/2) * (W/nf + 0.18u)' ps='2*int((nf+2)/2) * (W/nf + 0.18u)' nrd='0.18u / W' nrs='0.18u / W'
+ sa=0 sb=0 sd=0 m=1
XM81 D G S B nfet_03v3 L=0.28u W=0.25u nf=1 ad='int((nf+1)/2) * W/nf * 0.18u' as='int((nf+2)/2) * W/nf * 0.18u'
+ pd='2*int((nf+1)/2) * (W/nf + 0.18u)' ps='2*int((nf+2)/2) * (W/nf + 0.18u)' nrd='0.18u / W' nrs='0.18u / W'
+ sa=0 sb=0 sd=0 m=1
XM82 D G S B nfet_03v3 L=0.28u W=0.25u nf=1 ad='int((nf+1)/2) * W/nf * 0.18u' as='int((nf+2)/2) * W/nf * 0.18u'
+ pd='2*int((nf+1)/2) * (W/nf + 0.18u)' ps='2*int((nf+2)/2) * (W/nf + 0.18u)' nrd='0.18u / W' nrs='0.18u / W'
+ sa=0 sb=0 sd=0 m=1
XM83 D G S B nfet_03v3 L=0.28u W=0.25u nf=1 ad='int((nf+1)/2) * W/nf * 0.18u' as='int((nf+2)/2) * W/nf * 0.18u'
+ pd='2*int((nf+1)/2) * (W/nf + 0.18u)' ps='2*int((nf+2)/2) * (W/nf + 0.18u)' nrd='0.18u / W' nrs='0.18u / W'
+ sa=0 sb=0 sd=0 m=1
XM84 D G S B nfet_03v3 L=0.28u W=0.25u nf=1 ad='int((nf+1)/2) * W/nf * 0.18u' as='int((nf+2)/2) * W/nf * 0.18u'
+ pd='2*int((nf+1)/2) * (W/nf + 0.18u)' ps='2*int((nf+2)/2) * (W/nf + 0.18u)' nrd='0.18u / W' nrs='0.18u / W'
+ sa=0 sb=0 sd=0 m=1
XM85 D G S B nfet_03v3 L=0.28u W=0.25u nf=1 ad='int((nf+1)/2) * W/nf * 0.18u' as='int((nf+2)/2) * W/nf * 0.18u'
+ pd='2*int((nf+1)/2) * (W/nf + 0.18u)' ps='2*int((nf+2)/2) * (W/nf + 0.18u)' nrd='0.18u / W' nrs='0.18u / W'
+ sa=0 sb=0 sd=0 m=1
XM86 D G S B nfet_03v3 L=0.28u W=0.25u nf=1 ad='int((nf+1)/2) * W/nf * 0.18u' as='int((nf+2)/2) * W/nf * 0.18u'
+ pd='2*int((nf+1)/2) * (W/nf + 0.18u)' ps='2*int((nf+2)/2) * (W/nf + 0.18u)' nrd='0.18u / W' nrs='0.18u / W'
+ sa=0 sb=0 sd=0 m=1
XM87 D G S B nfet_03v3 L=0.28u W=0.25u nf=1 ad='int((nf+1)/2) * W/nf * 0.18u' as='int((nf+2)/2) * W/nf * 0.18u'
+ pd='2*int((nf+1)/2) * (W/nf + 0.18u)' ps='2*int((nf+2)/2) * (W/nf + 0.18u)' nrd='0.18u / W' nrs='0.18u / W'
+ sa=0 sb=0 sd=0 m=1
XM88 D G S B nfet_03v3 L=0.28u W=0.25u nf=1 ad='int((nf+1)/2) * W/nf * 0.18u' as='int((nf+2)/2) * W/nf * 0.18u'
+ pd='2*int((nf+1)/2) * (W/nf + 0.18u)' ps='2*int((nf+2)/2) * (W/nf + 0.18u)' nrd='0.18u / W' nrs='0.18u / W'
+ sa=0 sb=0 sd=0 m=1
XM89 D G S B nfet_03v3 L=0.28u W=0.25u nf=1 ad='int((nf+1)/2) * W/nf * 0.18u' as='int((nf+2)/2) * W/nf * 0.18u'
+ pd='2*int((nf+1)/2) * (W/nf + 0.18u)' ps='2*int((nf+2)/2) * (W/nf + 0.18u)' nrd='0.18u / W' nrs='0.18u / W'
+ sa=0 sb=0 sd=0 m=1
XM90 D G S B nfet_03v3 L=0.28u W=0.25u nf=1 ad='int((nf+1)/2) * W/nf * 0.18u' as='int((nf+2)/2) * W/nf * 0.18u'
+ pd='2*int((nf+1)/2) * (W/nf + 0.18u)' ps='2*int((nf+2)/2) * (W/nf + 0.18u)' nrd='0.18u / W' nrs='0.18u / W'
+ sa=0 sb=0 sd=0 m=1
XM91 D G S B nfet_03v3 L=0.28u W=0.25u nf=1 ad='int((nf+1)/2) * W/nf * 0.18u' as='int((nf+2)/2) * W/nf * 0.18u'
+ pd='2*int((nf+1)/2) * (W/nf + 0.18u)' ps='2*int((nf+2)/2) * (W/nf + 0.18u)' nrd='0.18u / W' nrs='0.18u / W'
+ sa=0 sb=0 sd=0 m=1
XM92 D G S B nfet_03v3 L=0.28u W=0.25u nf=1 ad='int((nf+1)/2) * W/nf * 0.18u' as='int((nf+2)/2) * W/nf * 0.18u'
+ pd='2*int((nf+1)/2) * (W/nf + 0.18u)' ps='2*int((nf+2)/2) * (W/nf + 0.18u)' nrd='0.18u / W' nrs='0.18u / W'
+ sa=0 sb=0 sd=0 m=1
XM93 D G S B nfet_03v3 L=0.28u W=0.25u nf=1 ad='int((nf+1)/2) * W/nf * 0.18u' as='int((nf+2)/2) * W/nf * 0.18u'
+ pd='2*int((nf+1)/2) * (W/nf + 0.18u)' ps='2*int((nf+2)/2) * (W/nf + 0.18u)' nrd='0.18u / W' nrs='0.18u / W'
+ sa=0 sb=0 sd=0 m=1
XM94 D G S B nfet_03v3 L=0.28u W=0.25u nf=1 ad='int((nf+1)/2) * W/nf * 0.18u' as='int((nf+2)/2) * W/nf * 0.18u'
+ pd='2*int((nf+1)/2) * (W/nf + 0.18u)' ps='2*int((nf+2)/2) * (W/nf + 0.18u)' nrd='0.18u / W' nrs='0.18u / W'
+ sa=0 sb=0 sd=0 m=1
XM95 D G S B nfet_03v3 L=0.28u W=0.25u nf=1 ad='int((nf+1)/2) * W/nf * 0.18u' as='int((nf+2)/2) * W/nf * 0.18u'
+ pd='2*int((nf+1)/2) * (W/nf + 0.18u)' ps='2*int((nf+2)/2) * (W/nf + 0.18u)' nrd='0.18u / W' nrs='0.18u / W'
+ sa=0 sb=0 sd=0 m=1
XM96 D G S B nfet_03v3 L=0.28u W=0.25u nf=1 ad='int((nf+1)/2) * W/nf * 0.18u' as='int((nf+2)/2) * W/nf * 0.18u'
+ pd='2*int((nf+1)/2) * (W/nf + 0.18u)' ps='2*int((nf+2)/2) * (W/nf + 0.18u)' nrd='0.18u / W' nrs='0.18u / W'
+ sa=0 sb=0 sd=0 m=1
XM97 D G S B nfet_03v3 L=0.28u W=0.25u nf=1 ad='int((nf+1)/2) * W/nf * 0.18u' as='int((nf+2)/2) * W/nf * 0.18u'
+ pd='2*int((nf+1)/2) * (W/nf + 0.18u)' ps='2*int((nf+2)/2) * (W/nf + 0.18u)' nrd='0.18u / W' nrs='0.18u / W'
+ sa=0 sb=0 sd=0 m=1
XM98 D G S B nfet_03v3 L=0.28u W=0.25u nf=1 ad='int((nf+1)/2) * W/nf * 0.18u' as='int((nf+2)/2) * W/nf * 0.18u'
+ pd='2*int((nf+1)/2) * (W/nf + 0.18u)' ps='2*int((nf+2)/2) * (W/nf + 0.18u)' nrd='0.18u / W' nrs='0.18u / W'
+ sa=0 sb=0 sd=0 m=1
XM99 D G S B nfet_03v3 L=0.28u W=0.25u nf=1 ad='int((nf+1)/2) * W/nf * 0.18u' as='int((nf+2)/2) * W/nf * 0.18u'
+ pd='2*int((nf+1)/2) * (W/nf + 0.18u)' ps='2*int((nf+2)/2) * (W/nf + 0.18u)' nrd='0.18u / W' nrs='0.18u / W'
+ sa=0 sb=0 sd=0 m=1
XM100 D G S B nfet_03v3 L=0.28u W=0.25u nf=1 ad='int((nf+1)/2) * W/nf * 0.18u' as='int((nf+2)/2) * W/nf * 0.18u'
+ pd='2*int((nf+1)/2) * (W/nf + 0.18u)' ps='2*int((nf+2)/2) * (W/nf + 0.18u)' nrd='0.18u / W' nrs='0.18u / W'
+ sa=0 sb=0 sd=0 m=1
XM101 D G S B nfet_03v3 L=0.28u W=0.25u nf=1 ad='int((nf+1)/2) * W/nf * 0.18u' as='int((nf+2)/2) * W/nf * 0.18u'
+ pd='2*int((nf+1)/2) * (W/nf + 0.18u)' ps='2*int((nf+2)/2) * (W/nf + 0.18u)' nrd='0.18u / W' nrs='0.18u / W'
+ sa=0 sb=0 sd=0 m=1
XM102 D G S B nfet_03v3 L=0.28u W=0.25u nf=1 ad='int((nf+1)/2) * W/nf * 0.18u' as='int((nf+2)/2) * W/nf * 0.18u'
+ pd='2*int((nf+1)/2) * (W/nf + 0.18u)' ps='2*int((nf+2)/2) * (W/nf + 0.18u)' nrd='0.18u / W' nrs='0.18u / W'
+ sa=0 sb=0 sd=0 m=1
XM103 D G S B nfet_03v3 L=0.28u W=0.25u nf=1 ad='int((nf+1)/2) * W/nf * 0.18u' as='int((nf+2)/2) * W/nf * 0.18u'
+ pd='2*int((nf+1)/2) * (W/nf + 0.18u)' ps='2*int((nf+2)/2) * (W/nf + 0.18u)' nrd='0.18u / W' nrs='0.18u / W'
+ sa=0 sb=0 sd=0 m=1
XM104 D G S B nfet_03v3 L=0.28u W=0.25u nf=1 ad='int((nf+1)/2) * W/nf * 0.18u' as='int((nf+2)/2) * W/nf * 0.18u'
+ pd='2*int((nf+1)/2) * (W/nf + 0.18u)' ps='2*int((nf+2)/2) * (W/nf + 0.18u)' nrd='0.18u / W' nrs='0.18u / W'
+ sa=0 sb=0 sd=0 m=1
XM105 D G S B nfet_03v3 L=0.28u W=0.25u nf=1 ad='int((nf+1)/2) * W/nf * 0.18u' as='int((nf+2)/2) * W/nf * 0.18u'
+ pd='2*int((nf+1)/2) * (W/nf + 0.18u)' ps='2*int((nf+2)/2) * (W/nf + 0.18u)' nrd='0.18u / W' nrs='0.18u / W'
+ sa=0 sb=0 sd=0 m=1
XM106 D G S B nfet_03v3 L=0.28u W=0.25u nf=1 ad='int((nf+1)/2) * W/nf * 0.18u' as='int((nf+2)/2) * W/nf * 0.18u'
+ pd='2*int((nf+1)/2) * (W/nf + 0.18u)' ps='2*int((nf+2)/2) * (W/nf + 0.18u)' nrd='0.18u / W' nrs='0.18u / W'
+ sa=0 sb=0 sd=0 m=1
XM107 D G S B nfet_03v3 L=0.28u W=0.25u nf=1 ad='int((nf+1)/2) * W/nf * 0.18u' as='int((nf+2)/2) * W/nf * 0.18u'
+ pd='2*int((nf+1)/2) * (W/nf + 0.18u)' ps='2*int((nf+2)/2) * (W/nf + 0.18u)' nrd='0.18u / W' nrs='0.18u / W'
+ sa=0 sb=0 sd=0 m=1
XM108 D G S B nfet_03v3 L=0.28u W=0.25u nf=1 ad='int((nf+1)/2) * W/nf * 0.18u' as='int((nf+2)/2) * W/nf * 0.18u'
+ pd='2*int((nf+1)/2) * (W/nf + 0.18u)' ps='2*int((nf+2)/2) * (W/nf + 0.18u)' nrd='0.18u / W' nrs='0.18u / W'
+ sa=0 sb=0 sd=0 m=1
XM109 D G S B nfet_03v3 L=0.28u W=0.25u nf=1 ad='int((nf+1)/2) * W/nf * 0.18u' as='int((nf+2)/2) * W/nf * 0.18u'
+ pd='2*int((nf+1)/2) * (W/nf + 0.18u)' ps='2*int((nf+2)/2) * (W/nf + 0.18u)' nrd='0.18u / W' nrs='0.18u / W'
+ sa=0 sb=0 sd=0 m=1
XM110 D G S B nfet_03v3 L=0.28u W=0.25u nf=1 ad='int((nf+1)/2) * W/nf * 0.18u' as='int((nf+2)/2) * W/nf * 0.18u'
+ pd='2*int((nf+1)/2) * (W/nf + 0.18u)' ps='2*int((nf+2)/2) * (W/nf + 0.18u)' nrd='0.18u / W' nrs='0.18u / W'
+ sa=0 sb=0 sd=0 m=1
XM111 D G S B nfet_03v3 L=0.28u W=0.25u nf=1 ad='int((nf+1)/2) * W/nf * 0.18u' as='int((nf+2)/2) * W/nf * 0.18u'
+ pd='2*int((nf+1)/2) * (W/nf + 0.18u)' ps='2*int((nf+2)/2) * (W/nf + 0.18u)' nrd='0.18u / W' nrs='0.18u / W'
+ sa=0 sb=0 sd=0 m=1
XM112 D G S B nfet_03v3 L=0.28u W=0.25u nf=1 ad='int((nf+1)/2) * W/nf * 0.18u' as='int((nf+2)/2) * W/nf * 0.18u'
+ pd='2*int((nf+1)/2) * (W/nf + 0.18u)' ps='2*int((nf+2)/2) * (W/nf + 0.18u)' nrd='0.18u / W' nrs='0.18u / W'
+ sa=0 sb=0 sd=0 m=1
XM113 D G S B nfet_03v3 L=0.28u W=0.25u nf=1 ad='int((nf+1)/2) * W/nf * 0.18u' as='int((nf+2)/2) * W/nf * 0.18u'
+ pd='2*int((nf+1)/2) * (W/nf + 0.18u)' ps='2*int((nf+2)/2) * (W/nf + 0.18u)' nrd='0.18u / W' nrs='0.18u / W'
+ sa=0 sb=0 sd=0 m=1
XM114 D G S B nfet_03v3 L=0.28u W=0.25u nf=1 ad='int((nf+1)/2) * W/nf * 0.18u' as='int((nf+2)/2) * W/nf * 0.18u'
+ pd='2*int((nf+1)/2) * (W/nf + 0.18u)' ps='2*int((nf+2)/2) * (W/nf + 0.18u)' nrd='0.18u / W' nrs='0.18u / W'
+ sa=0 sb=0 sd=0 m=1
XM115 D G S B nfet_03v3 L=0.28u W=0.25u nf=1 ad='int((nf+1)/2) * W/nf * 0.18u' as='int((nf+2)/2) * W/nf * 0.18u'
+ pd='2*int((nf+1)/2) * (W/nf + 0.18u)' ps='2*int((nf+2)/2) * (W/nf + 0.18u)' nrd='0.18u / W' nrs='0.18u / W'
+ sa=0 sb=0 sd=0 m=1
XM116 D G S B nfet_03v3 L=0.28u W=0.25u nf=1 ad='int((nf+1)/2) * W/nf * 0.18u' as='int((nf+2)/2) * W/nf * 0.18u'
+ pd='2*int((nf+1)/2) * (W/nf + 0.18u)' ps='2*int((nf+2)/2) * (W/nf + 0.18u)' nrd='0.18u / W' nrs='0.18u / W'
+ sa=0 sb=0 sd=0 m=1
XM117 D G S B nfet_03v3 L=0.28u W=0.25u nf=1 ad='int((nf+1)/2) * W/nf * 0.18u' as='int((nf+2)/2) * W/nf * 0.18u'
+ pd='2*int((nf+1)/2) * (W/nf + 0.18u)' ps='2*int((nf+2)/2) * (W/nf + 0.18u)' nrd='0.18u / W' nrs='0.18u / W'
+ sa=0 sb=0 sd=0 m=1
XM118 D G S B nfet_03v3 L=0.28u W=0.25u nf=1 ad='int((nf+1)/2) * W/nf * 0.18u' as='int((nf+2)/2) * W/nf * 0.18u'
+ pd='2*int((nf+1)/2) * (W/nf + 0.18u)' ps='2*int((nf+2)/2) * (W/nf + 0.18u)' nrd='0.18u / W' nrs='0.18u / W'
+ sa=0 sb=0 sd=0 m=1
XM119 D G S B nfet_03v3 L=0.28u W=0.25u nf=1 ad='int((nf+1)/2) * W/nf * 0.18u' as='int((nf+2)/2) * W/nf * 0.18u'
+ pd='2*int((nf+1)/2) * (W/nf + 0.18u)' ps='2*int((nf+2)/2) * (W/nf + 0.18u)' nrd='0.18u / W' nrs='0.18u / W'
+ sa=0 sb=0 sd=0 m=1
XM120 D G S B nfet_03v3 L=0.28u W=0.25u nf=1 ad='int((nf+1)/2) * W/nf * 0.18u' as='int((nf+2)/2) * W/nf * 0.18u'
+ pd='2*int((nf+1)/2) * (W/nf + 0.18u)' ps='2*int((nf+2)/2) * (W/nf + 0.18u)' nrd='0.18u / W' nrs='0.18u / W'
+ sa=0 sb=0 sd=0 m=1
XM121 D G S B nfet_03v3 L=0.28u W=0.25u nf=1 ad='int((nf+1)/2) * W/nf * 0.18u' as='int((nf+2)/2) * W/nf * 0.18u'
+ pd='2*int((nf+1)/2) * (W/nf + 0.18u)' ps='2*int((nf+2)/2) * (W/nf + 0.18u)' nrd='0.18u / W' nrs='0.18u / W'
+ sa=0 sb=0 sd=0 m=1
XM122 D G S B nfet_03v3 L=0.28u W=0.25u nf=1 ad='int((nf+1)/2) * W/nf * 0.18u' as='int((nf+2)/2) * W/nf * 0.18u'
+ pd='2*int((nf+1)/2) * (W/nf + 0.18u)' ps='2*int((nf+2)/2) * (W/nf + 0.18u)' nrd='0.18u / W' nrs='0.18u / W'
+ sa=0 sb=0 sd=0 m=1
XM123 D G S B nfet_03v3 L=0.28u W=0.25u nf=1 ad='int((nf+1)/2) * W/nf * 0.18u' as='int((nf+2)/2) * W/nf * 0.18u'
+ pd='2*int((nf+1)/2) * (W/nf + 0.18u)' ps='2*int((nf+2)/2) * (W/nf + 0.18u)' nrd='0.18u / W' nrs='0.18u / W'
+ sa=0 sb=0 sd=0 m=1
XM124 D G S B nfet_03v3 L=0.28u W=0.25u nf=1 ad='int((nf+1)/2) * W/nf * 0.18u' as='int((nf+2)/2) * W/nf * 0.18u'
+ pd='2*int((nf+1)/2) * (W/nf + 0.18u)' ps='2*int((nf+2)/2) * (W/nf + 0.18u)' nrd='0.18u / W' nrs='0.18u / W'
+ sa=0 sb=0 sd=0 m=1
XM125 D G S B nfet_03v3 L=0.28u W=0.25u nf=1 ad='int((nf+1)/2) * W/nf * 0.18u' as='int((nf+2)/2) * W/nf * 0.18u'
+ pd='2*int((nf+1)/2) * (W/nf + 0.18u)' ps='2*int((nf+2)/2) * (W/nf + 0.18u)' nrd='0.18u / W' nrs='0.18u / W'
+ sa=0 sb=0 sd=0 m=1
XM126 D G S B nfet_03v3 L=0.28u W=0.25u nf=1 ad='int((nf+1)/2) * W/nf * 0.18u' as='int((nf+2)/2) * W/nf * 0.18u'
+ pd='2*int((nf+1)/2) * (W/nf + 0.18u)' ps='2*int((nf+2)/2) * (W/nf + 0.18u)' nrd='0.18u / W' nrs='0.18u / W'
+ sa=0 sb=0 sd=0 m=1
XM127 D G S B nfet_03v3 L=0.28u W=0.25u nf=1 ad='int((nf+1)/2) * W/nf * 0.18u' as='int((nf+2)/2) * W/nf * 0.18u'
+ pd='2*int((nf+1)/2) * (W/nf + 0.18u)' ps='2*int((nf+2)/2) * (W/nf + 0.18u)' nrd='0.18u / W' nrs='0.18u / W'
+ sa=0 sb=0 sd=0 m=1
XM128 D G S B nfet_03v3 L=0.28u W=0.25u nf=1 ad='int((nf+1)/2) * W/nf * 0.18u' as='int((nf+2)/2) * W/nf * 0.18u'
+ pd='2*int((nf+1)/2) * (W/nf + 0.18u)' ps='2*int((nf+2)/2) * (W/nf + 0.18u)' nrd='0.18u / W' nrs='0.18u / W'
+ sa=0 sb=0 sd=0 m=1
**.ends
.end
